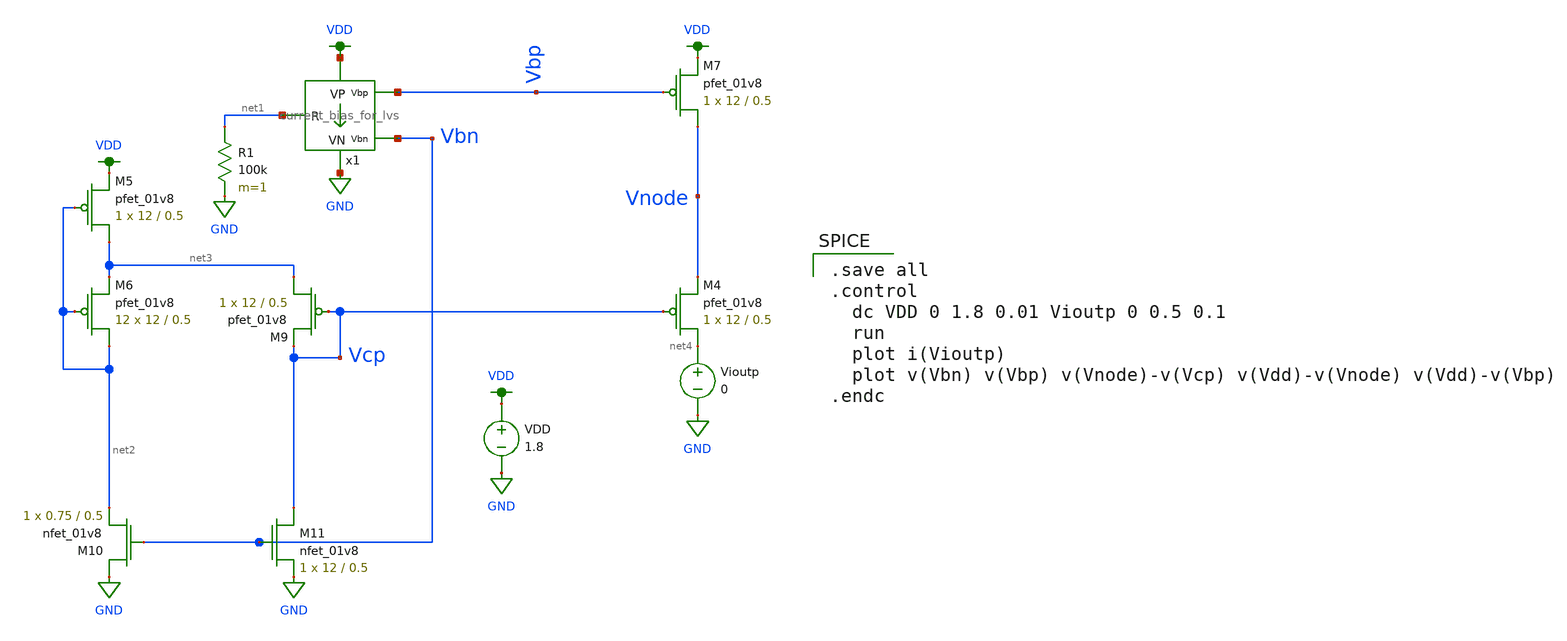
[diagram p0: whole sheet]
** sch_path: mp4_submission/bias_gen/simulations/test_lvs_current_bias.sch
**.subckt test_lvs_current_bias
VDD VDD GND 1.8
Vioutp net4 GND 0
R1 net1 GND 100k m=1
x1 VDD GND Vbp Vbn net1 current_bias_for_lvs
XM5 net3 net2 VDD VDD sky130_fd_pr__pfet_01v8 L=0.5 W=12 nf=1 ad='int((nf+1)/2) * W/nf * 0.29' as='int((nf+2)/2) * W/nf * 0.29'
+ pd='2*int((nf+1)/2) * (W/nf + 0.29)' ps='2*int((nf+2)/2) * (W/nf + 0.29)' nrd='0.29 / W' nrs='0.29 / W'
+ sa=0 sb=0 sd=0 mult=1 m=1
XM6 net2 net2 net3 VDD sky130_fd_pr__pfet_01v8 L=0.5 W=12 nf=1 ad='int((nf+1)/2) * W/nf * 0.29' as='int((nf+2)/2) * W/nf * 0.29'
+ pd='2*int((nf+1)/2) * (W/nf + 0.29)' ps='2*int((nf+2)/2) * (W/nf + 0.29)' nrd='0.29 / W' nrs='0.29 / W'
+ sa=0 sb=0 sd=0 mult=12 m=12
XM9 net3 Vcp Vcp VDD sky130_fd_pr__pfet_01v8 L=0.5 W=12 nf=1 ad='int((nf+1)/2) * W/nf * 0.29' as='int((nf+2)/2) * W/nf * 0.29'
+ pd='2*int((nf+1)/2) * (W/nf + 0.29)' ps='2*int((nf+2)/2) * (W/nf + 0.29)' nrd='0.29 / W' nrs='0.29 / W'
+ sa=0 sb=0 sd=0 mult=1 m=1
XM10 GND Vbn net2 GND sky130_fd_pr__nfet_01v8 L=0.5 W=0.75 nf=1 ad='int((nf+1)/2) * W/nf * 0.29' as='int((nf+2)/2) * W/nf * 0.29'
+ pd='2*int((nf+1)/2) * (W/nf + 0.29)' ps='2*int((nf+2)/2) * (W/nf + 0.29)' nrd='0.29 / W' nrs='0.29 / W'
+ sa=0 sb=0 sd=0 mult=1 m=1
XM11 Vcp Vbn GND GND sky130_fd_pr__nfet_01v8 L=0.5 W=12 nf=1 ad='int((nf+1)/2) * W/nf * 0.29' as='int((nf+2)/2) * W/nf * 0.29'
+ pd='2*int((nf+1)/2) * (W/nf + 0.29)' ps='2*int((nf+2)/2) * (W/nf + 0.29)' nrd='0.29 / W' nrs='0.29 / W'
+ sa=0 sb=0 sd=0 mult=1 m=1
XM4 net4 Vcp Vnode VDD sky130_fd_pr__pfet_01v8 L=0.5 W=12 nf=1 ad='int((nf+1)/2) * W/nf * 0.29' as='int((nf+2)/2) * W/nf * 0.29'
+ pd='2*int((nf+1)/2) * (W/nf + 0.29)' ps='2*int((nf+2)/2) * (W/nf + 0.29)' nrd='0.29 / W' nrs='0.29 / W'
+ sa=0 sb=0 sd=0 mult=1 m=1
XM7 Vnode Vbp VDD VDD sky130_fd_pr__pfet_01v8 L=0.5 W=12 nf=1 ad='int((nf+1)/2) * W/nf * 0.29' as='int((nf+2)/2) * W/nf * 0.29'
+ pd='2*int((nf+1)/2) * (W/nf + 0.29)' ps='2*int((nf+2)/2) * (W/nf + 0.29)' nrd='0.29 / W' nrs='0.29 / W'
+ sa=0 sb=0 sd=0 mult=1 m=1
**** begin user architecture code

.option wnflag=1
.param MC_SWITCH=1.0
.lib ~/skywater/skywater-pdk/libraries/sky130_fd_pr_ngspice/latest/models/sky130.lib.spice tt


.save all
.control
  dc VDD 0 1.8 0.01 Vioutp 0 0.5 0.1
  run
  plot i(Vioutp)
  plot v(Vbn) v(Vbp) v(Vnode)-v(Vcp) v(Vdd)-v(Vnode) v(Vdd)-v(Vbp)
.endc

**** end user architecture code
**.ends
.GLOBAL VDD
.GLOBAL GND
.end
